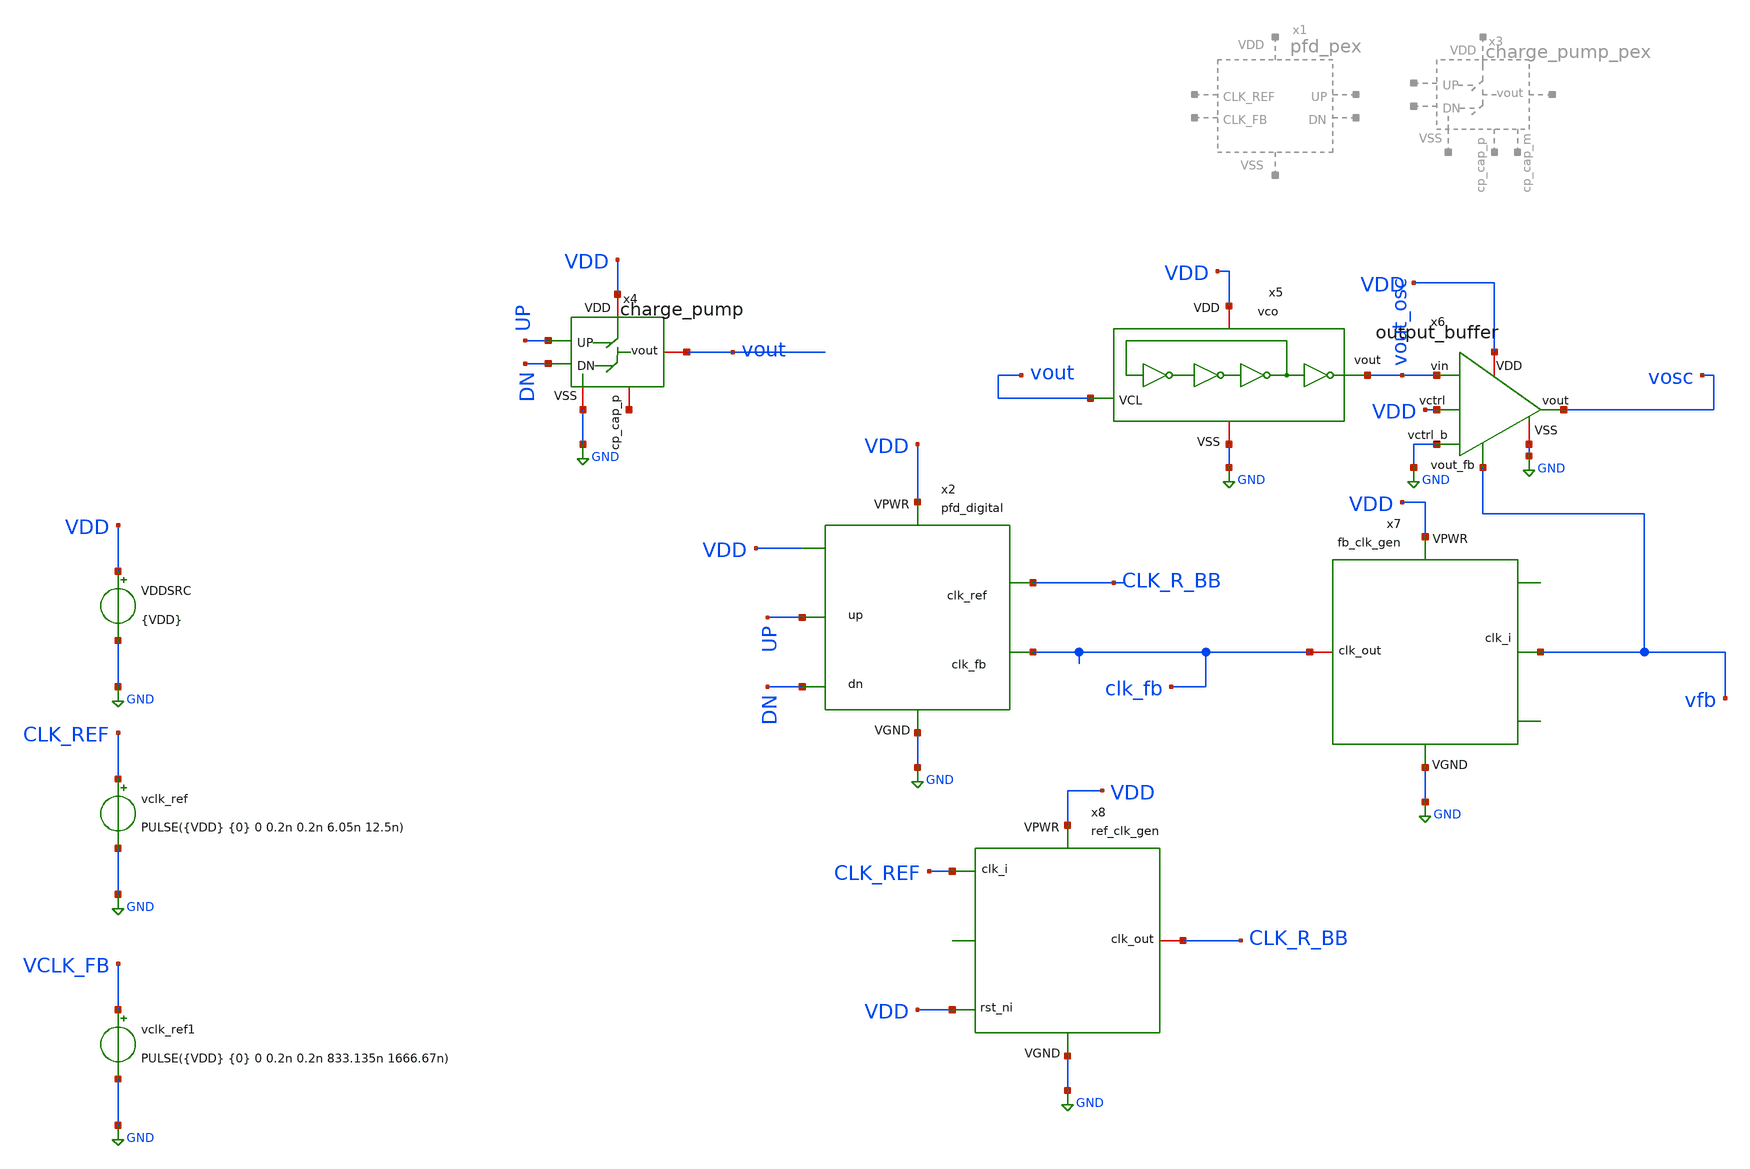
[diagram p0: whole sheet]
** sch_path: macros/heichips26_ook/macros/ook_analog_system/testbenches/xschem/charge_pump_tb_tran.sch
**.subckt charge_pump_tb_tran
VDDSRC VDD GND {VDD}
vclk_ref CLK_REF GND PULSE({VDD} {0} 0 0.2n 0.2n 6.05n 12.5n)
vclk_ref1 VCLK_FB GND PULSE({VDD} {0} 0 0.2n 0.2n 833.135n 1666.67n)
x2 VDD GND UP DN CLK_R_BB clk_fb pfd_digital
x4 net1 GND VDD UP vout DN charge_pump
x5 vout_osc VDD GND vout vco
x6 vfb VDD VDD vout_osc vosc GND GND output_buffer
x7 VDD GND vfb clk_fb fb_clk_gen
x8 VDD GND CLK_REF VDD CLK_R_BB ref_clk_gen
**** begin user architecture code


.param VDD=1.5
.param temp=27

.options klu method=gear trtol=25 reltol=1e-3 vntol=1e-6 gmin=1e-12 itl1=200 itl4=50
.control

save CLK_REF VCLK_FB UP DN vout vosc vfb clk_fb vout_osc CLK_R_BB

shell rm -f @schname\.raw
set wr_vecnames
set wr_singlescale

tran 10e-12 100e-6 0 10e-12
write @schname\.raw
wrdata ../plot_simulations/data/@schname\.txt v(CLK_REF) v(VCLK_FB) v(UP) v(DN) vout

plot UP DN
plot vout
plot vosc vfb clk_fb vout_osc
plot clk_fb
plot vosc
plot CLK_R_BB
.endc



.lib cornerMOSlv.lib mos_tt
.lib cornerMOShv.lib mos_tt
.lib cornerRES.lib res_typ
.lib cornerDIO.lib dio_tt
.lib cornerCAP.lib cap_typ
.include /home/belal/HeiChips/heichips26-on-off/macros/heichips26_ook/macros/ook_analog_system/netlist/pex/charge_pump_magic_pex_3.spice
.include /home/belal/HeiChips/heichips26-on-off/macros/heichips26_ook/macros/ook_analog_system/netlist/pex/pfd_magic_pex_3.spice
.include /home/belal/HeiChips/heichips26-on-off/macros/heichips26_ook/macros/pfd_digital/netlist/xspice/pfd_digital.xspice
.include /home/belal/HeiChips/heichips26-on-off/macros/heichips26_ook/macros/fb_clk_gen/netlist/xspice/fb_clk_gen.xspice
.include /home/belal/HeiChips/heichips26-on-off/macros/heichips26_ook/macros/ref_clk_gen/netlist/xspice/ref_clk_gen.xspice
.include /home/belal/HeiChips/heichips26-on-off/IHP-Open-PDK/ihp-sg13cmos5l/libs.tech/ngspice/models/cap_mfringe.lib

**** end user architecture code
**.ends
.GLOBAL GND
.end
